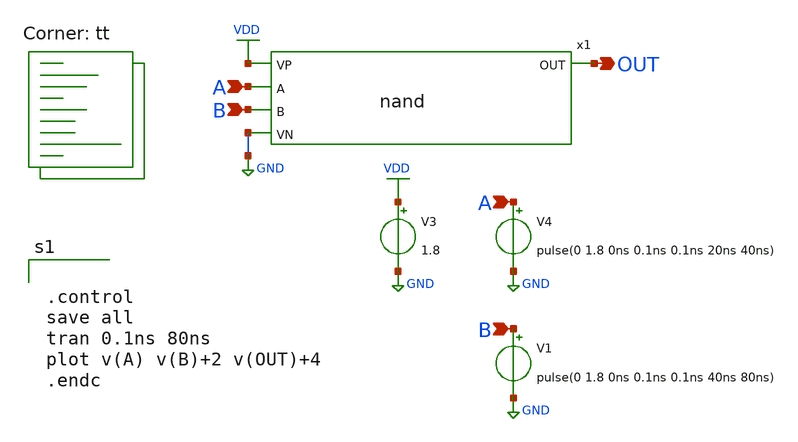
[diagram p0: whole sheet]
** sch_path: basic_cell/single_cell/nand/tb_xschem_nand.sch
**.subckt tb_xschem_nand A B A B OUT
*.ipin A
*.ipin B
*.ipin A
*.ipin B
*.opin OUT
V3 VDD GND 1.8
V4 A GND pulse(0 1.8 0ns 0.1ns 0.1ns 20ns 40ns)
V1 B GND pulse(0 1.8 0ns 0.1ns 0.1ns 40ns 80ns)
x1 VDD OUT A B GND nand
**** begin user architecture code
.lib $::SKYWATER_MODELS/sky130.lib.spice tt


.control
save all
tran 0.1ns 80ns
plot v(A) v(B)+2 v(OUT)+4
.endc


**** end user architecture code
**.ends

* expanding   symbol:  /foss/designs/APIC_Mux_DFF/basic_cell/single_cell/nand/nand.sym # of pins=5
** sym_path: basic_cell/single_cell/nand/nand.sym
** sch_path: basic_cell/single_cell/nand/nand.sch
.subckt nand VP OUT A B VN
*.ipin A
*.ipin B
*.opin OUT
*.ipin VN
*.ipin VP
XM4 OUT B net1 VN sky130_fd_pr__nfet_01v8 L=0.15 W=1 nf=1 ad='int((nf+1)/2) * W/nf * 0.29' as='int((nf+2)/2) * W/nf * 0.29'
+ pd='2*int((nf+1)/2) * (W/nf + 0.29)' ps='2*int((nf+2)/2) * (W/nf + 0.29)' nrd='0.29 / W' nrs='0.29 / W'
+ sa=0 sb=0 sd=0 mult=1 m=1
XM3 net1 A VN VN sky130_fd_pr__nfet_01v8 L=0.15 W=1 nf=1 ad='int((nf+1)/2) * W/nf * 0.29' as='int((nf+2)/2) * W/nf * 0.29'
+ pd='2*int((nf+1)/2) * (W/nf + 0.29)' ps='2*int((nf+2)/2) * (W/nf + 0.29)' nrd='0.29 / W' nrs='0.29 / W'
+ sa=0 sb=0 sd=0 mult=1 m=1
XM1 OUT B VP VP sky130_fd_pr__pfet_01v8 L=0.15 W=3 nf=1 ad='int((nf+1)/2) * W/nf * 0.29' as='int((nf+2)/2) * W/nf * 0.29'
+ pd='2*int((nf+1)/2) * (W/nf + 0.29)' ps='2*int((nf+2)/2) * (W/nf + 0.29)' nrd='0.29 / W' nrs='0.29 / W'
+ sa=0 sb=0 sd=0 mult=1 m=1
XM2 OUT A VP VP sky130_fd_pr__pfet_01v8 L=0.15 W=3 nf=1 ad='int((nf+1)/2) * W/nf * 0.29' as='int((nf+2)/2) * W/nf * 0.29'
+ pd='2*int((nf+1)/2) * (W/nf + 0.29)' ps='2*int((nf+2)/2) * (W/nf + 0.29)' nrd='0.29 / W' nrs='0.29 / W'
+ sa=0 sb=0 sd=0 mult=1 m=1
.ends

.GLOBAL VDD
.GLOBAL GND
.end
